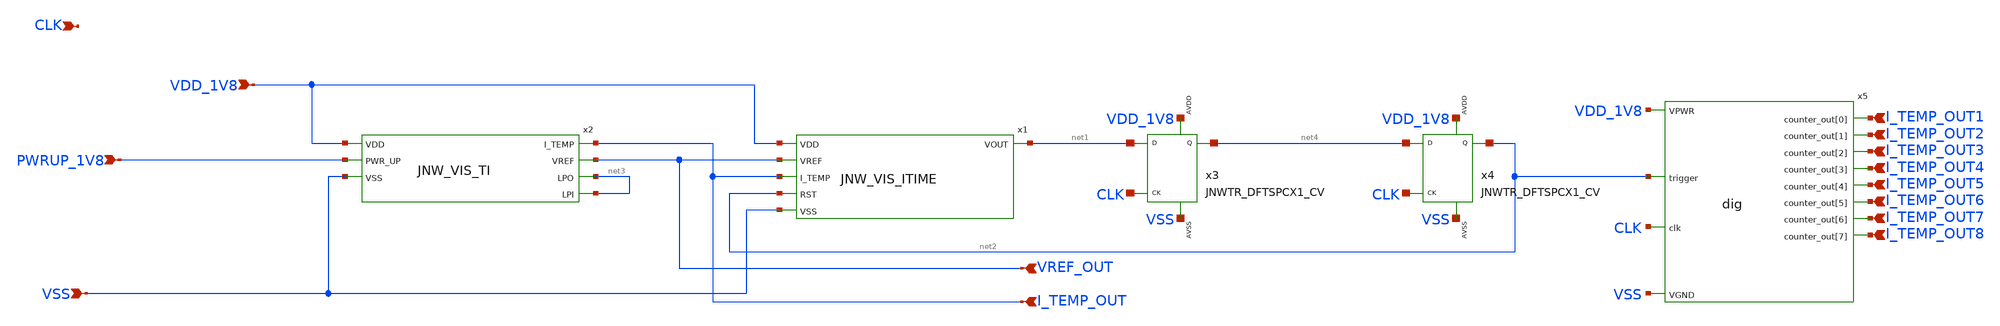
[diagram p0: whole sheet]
** sch_path: design/JNW_GR02_SKY130A/JNW_GR02.sch
**.subckt JNW_GR02 VDD_1V8 VSS PWRUP_1V8 I_TEMP_OUT VREF_OUT CLK I_TEMP_OUT8 I_TEMP_OUT7 I_TEMP_OUT6
*+ I_TEMP_OUT5 I_TEMP_OUT4 I_TEMP_OUT3 I_TEMP_OUT2 I_TEMP_OUT1
*.ipin VDD_1V8
*.ipin VSS
*.ipin PWRUP_1V8
*.ipin I_TEMP_OUT
*.ipin VREF_OUT
*.ipin CLK
*.ipin I_TEMP_OUT8
*.ipin I_TEMP_OUT7
*.ipin I_TEMP_OUT6
*.ipin I_TEMP_OUT5
*.ipin I_TEMP_OUT4
*.ipin I_TEMP_OUT3
*.ipin I_TEMP_OUT2
*.ipin I_TEMP_OUT1
x1 VDD_1V8 VREF_OUT net1 I_TEMP_OUT net2 VSS JNW_VIS_ITIME
x2 I_TEMP_OUT VDD_1V8 VREF_OUT net3 net3 PWRUP_1V8 VSS JNW_VIS_TI
x3 net1 CLK net4 VDD_1V8 VSS JNWTR_DFTSPCX1_CV xoffset=0 yoffset=0 angle=0
x4 net4 CLK net2 VDD_1V8 VSS JNWTR_DFTSPCX1_CV xoffset=0 yoffset=0 angle=0
x5 VSS VDD_1V8 CLK I_TEMP_OUT1 I_TEMP_OUT2 I_TEMP_OUT3 I_TEMP_OUT4 I_TEMP_OUT5 I_TEMP_OUT6
+ I_TEMP_OUT7 I_TEMP_OUT8 net2 dig
**** begin user architecture code



.include /home/georg/aicex/ip/jnw_gr02_sky130a/design/JNW_GR02_SKY130A/dig.spice




**** end user architecture code
**.ends
.end
